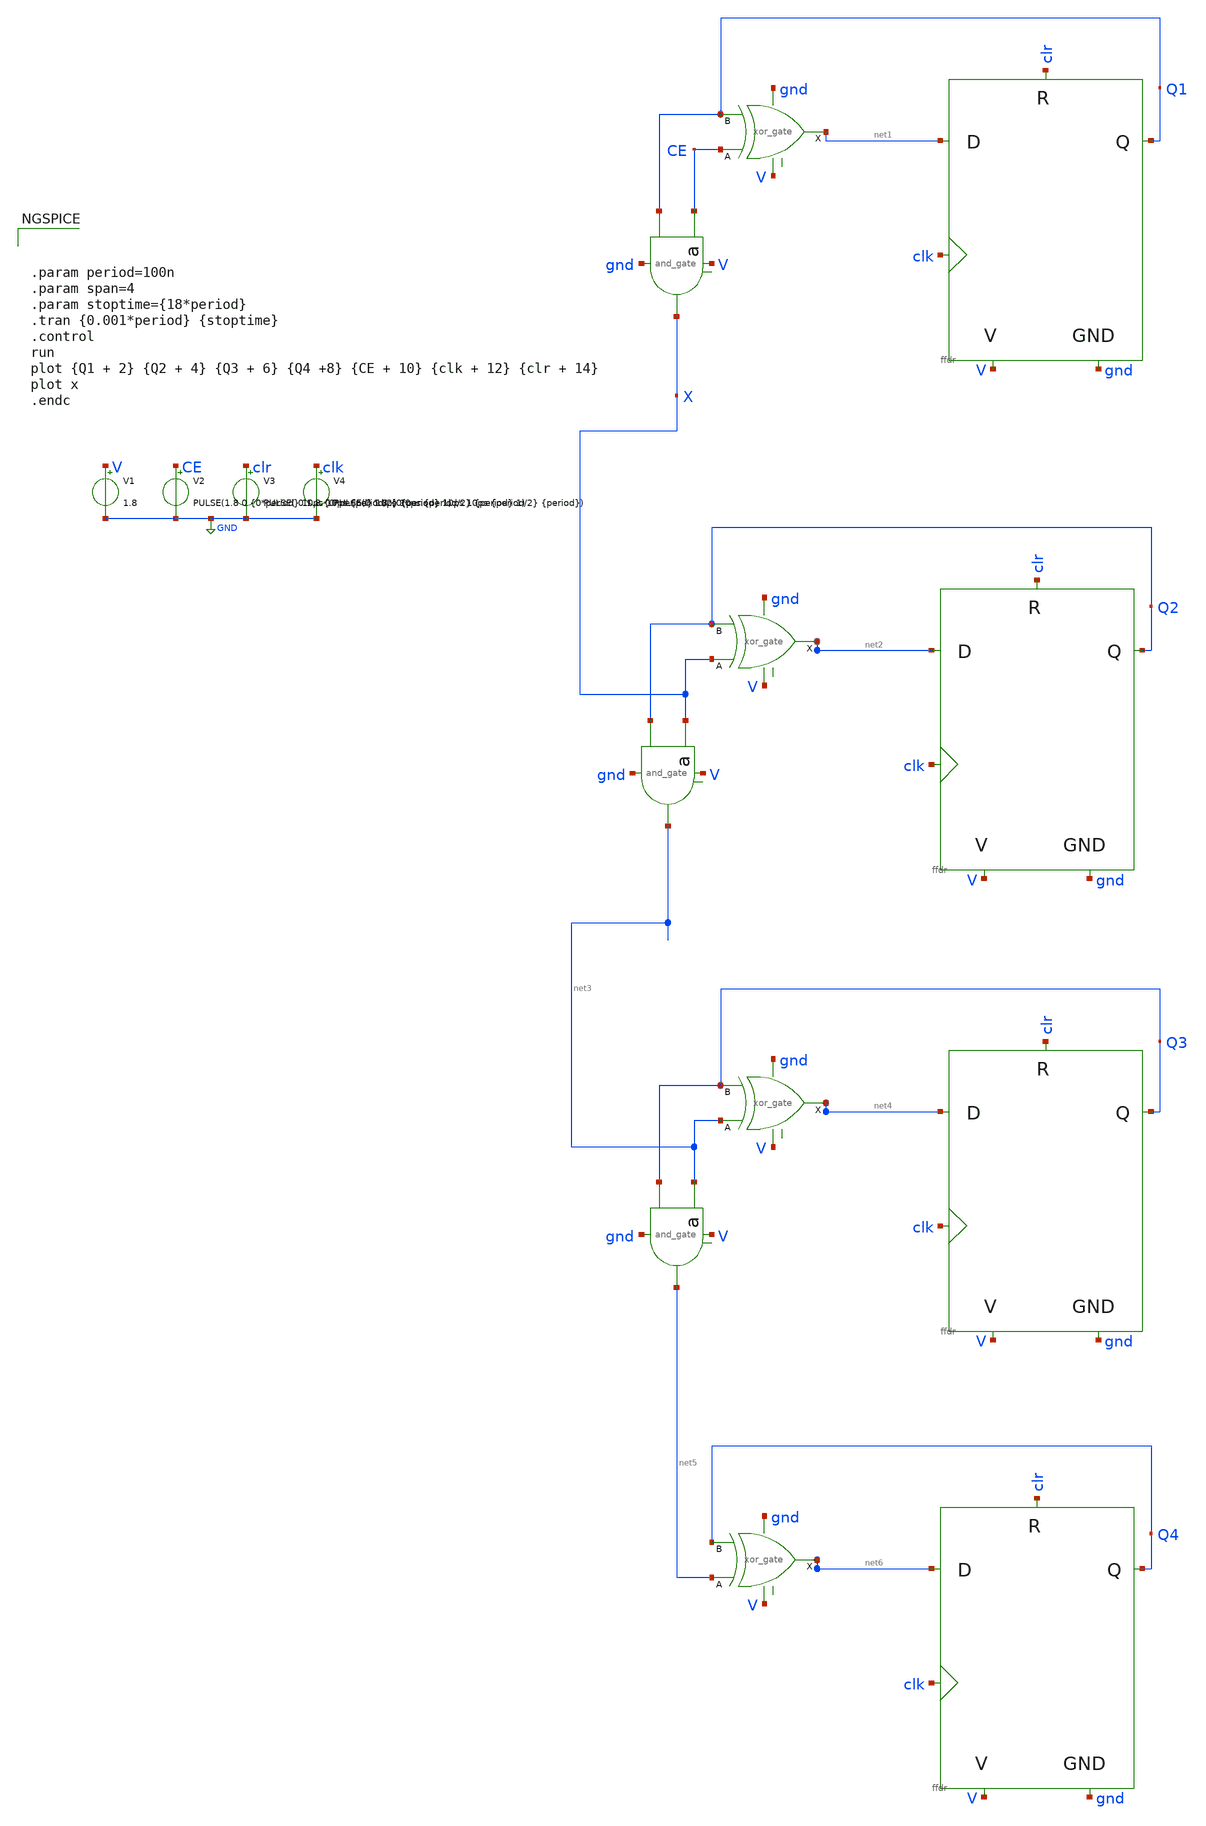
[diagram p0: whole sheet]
** sch_path: xschem/designs/counter4b/counter4b.sch
**.subckt counter4b
X1 CE Q1 gnd V X and_gate
X2 net1 clk V gnd Q1 clr ffdr
X3 CE Q1 net1 V gnd xor_gate
X4 X Q2 gnd V net3 and_gate
X5 net2 clk V gnd Q2 clr ffdr
X7 net3 Q3 gnd V net5 and_gate
X8 net4 clk V gnd Q3 clr ffdr
X11 net6 clk V gnd Q4 clr ffdr
V1 V GND 1.8
V2 CE GND PULSE(1.8 0 {0*period} 10ps 10ps {period/2} {period} 1)
V3 clr GND PULSE( 0 1.8 {0*period} 10ps 10ps {period/2} {period} 1)
V4 clk GND PULSE(0 1.8 {0*period} 10ps 10ps {period/2} {period})
X6 X Q2 net2 V gnd xor_gate
X9 net3 Q3 net4 V gnd xor_gate
X10 net5 Q4 net6 V gnd xor_gate
**** begin user architecture code



.param period=100n
.param span=4
.param stoptime={18*period}
.tran {0.001*period} {stoptime}
.control
run
plot {Q1 + 2} {Q2 + 4} {Q3 + 6} {Q4 +8} {CE + 10} {clk + 12} {clr + 14}
plot x
.endc


.lib $env(PDK_ROOT)/$env(PDK)/libs.tech/ngspice/sky130.lib.spice.tt.red tt


**** end user architecture code
**.ends
.GLOBAL GND
.end
